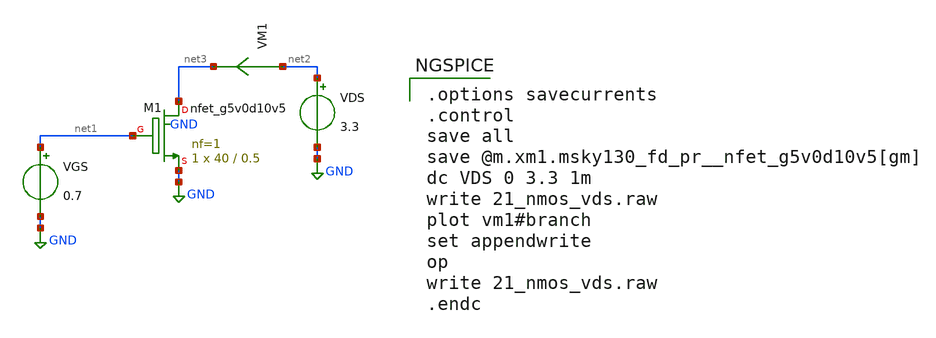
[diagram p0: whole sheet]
** sch_path: xschem/help/21_nmos_vds.sch
**.subckt 21_nmos_vds
XM1 net3 net1 GND GND sky130_fd_pr__nfet_g5v0d10v5 L=0.5 W=40 nf=1 ad='int((nf+1)/2) * W/nf * 0.29' as='int((nf+2)/2) * W/nf * 0.29'
+ pd='2*int((nf+1)/2) * (W/nf + 0.29)' ps='2*int((nf+2)/2) * (W/nf + 0.29)' nrd='0.29 / W' nrs='0.29 / W'
+ sa=0 sb=0 sd=0 mult=1 m=1
VGS net1 GND 0.7
VDS net2 GND 3.3
VM1 net2 net3 0
.save i(vm1)
**** begin user architecture code

.options savecurrents
.control
save all
save @m.xm1.msky130_fd_pr__nfet_g5v0d10v5[gm]
dc VDS 0 3.3 1m
write 21_nmos_vds.raw
plot vm1#branch
set appendwrite
op
write 21_nmos_vds.raw
.endc



** opencircuitdesign pdks install
.lib $::SKYWATER_MODELS/sky130.lib.spice tt


**** end user architecture code
**.ends
.GLOBAL GND
.end
